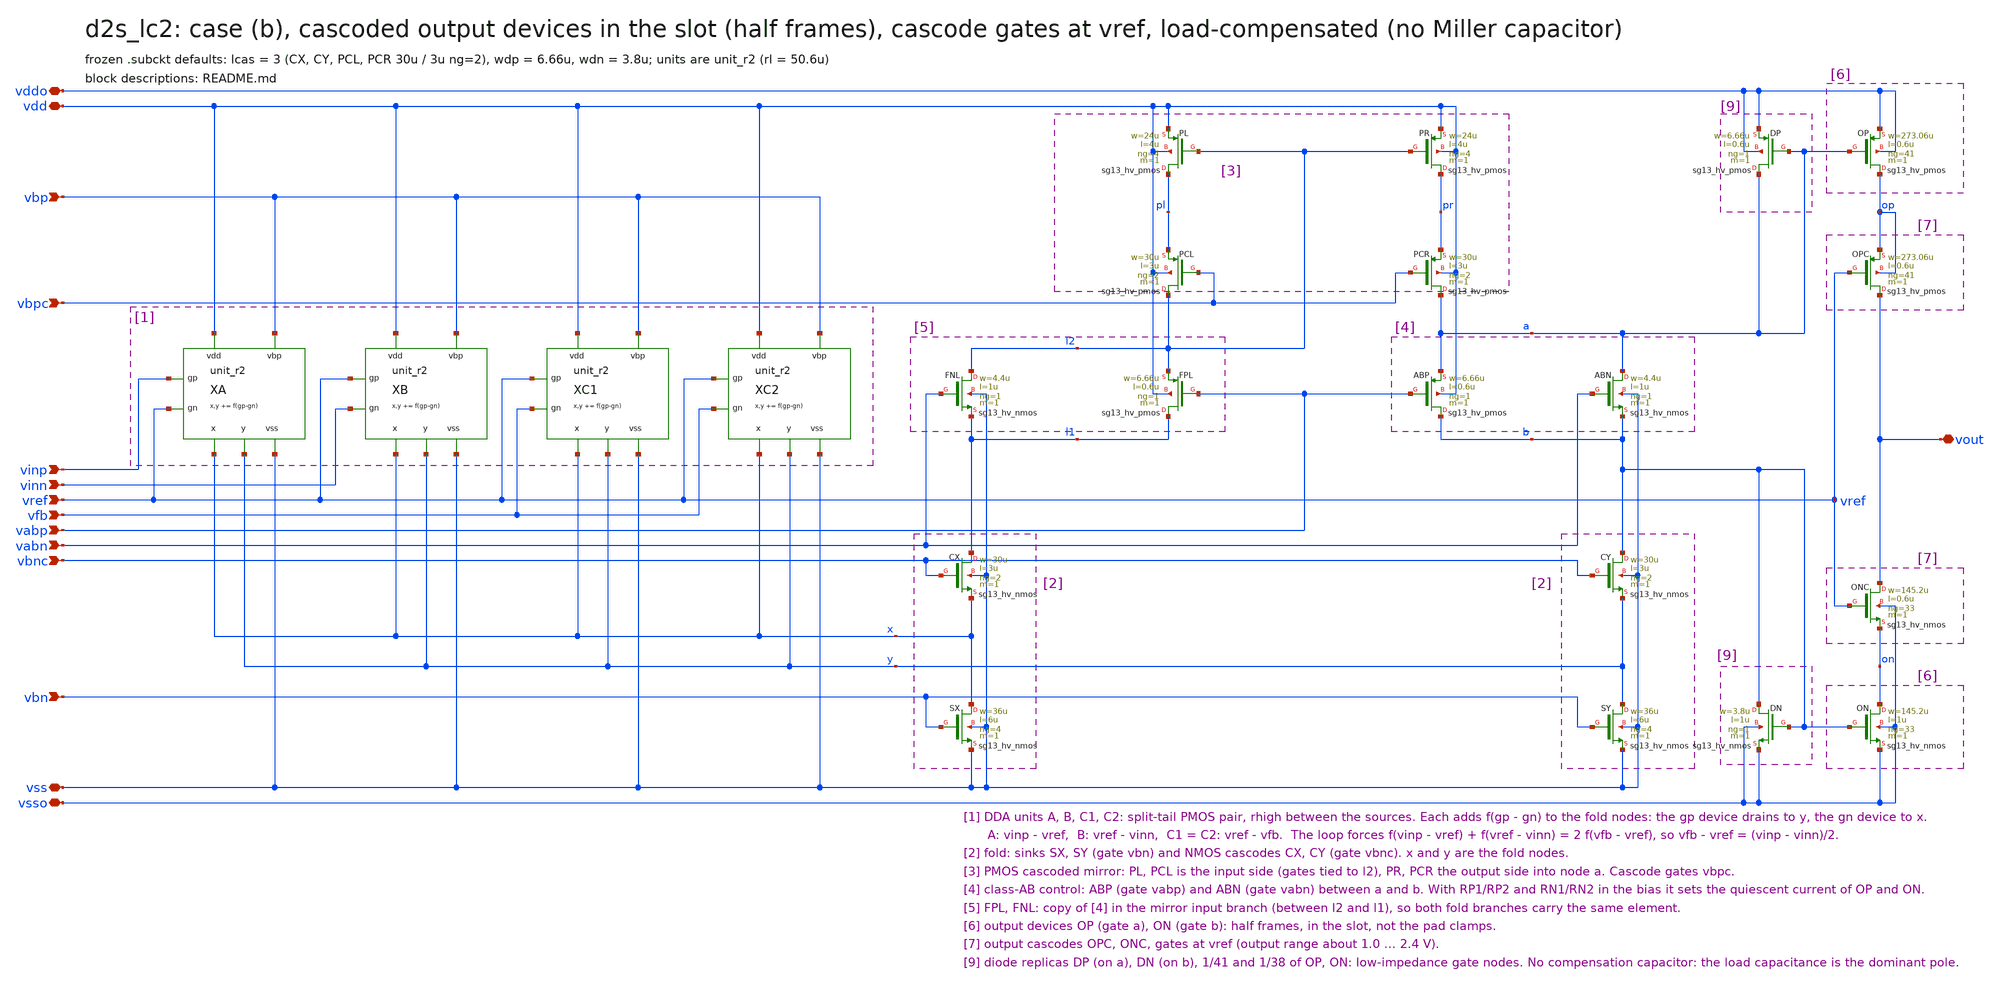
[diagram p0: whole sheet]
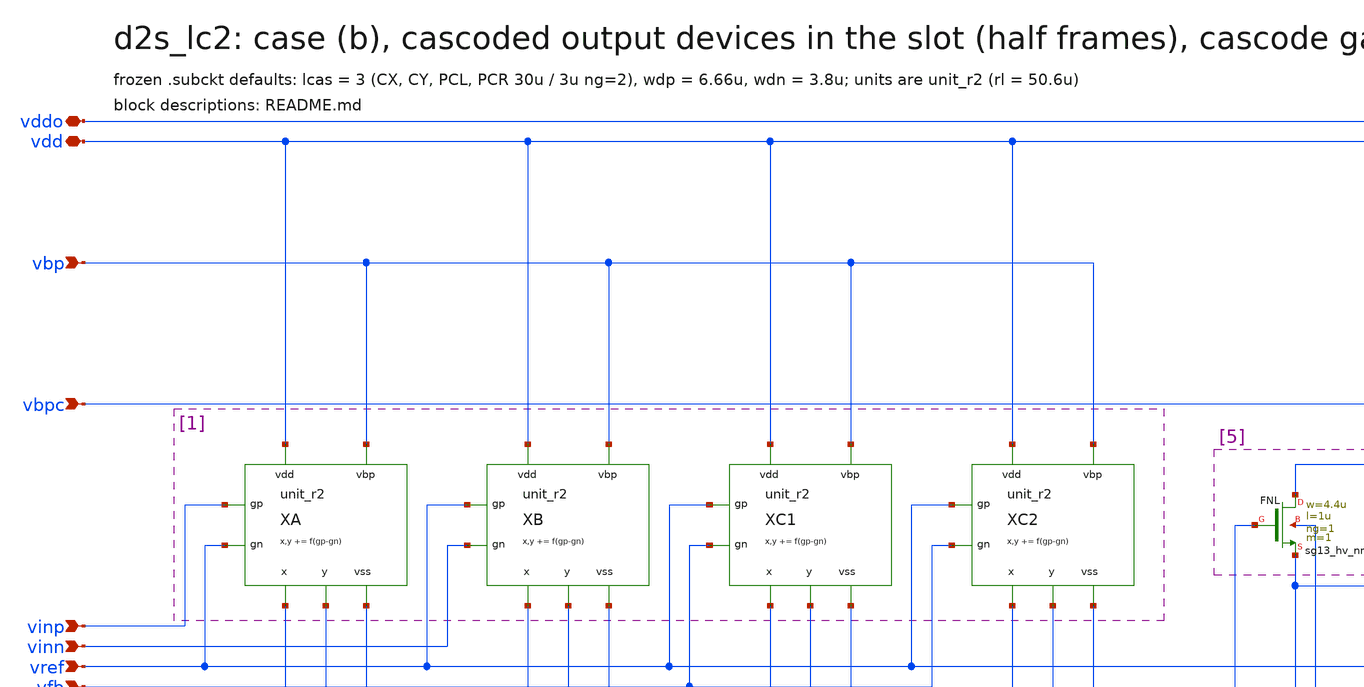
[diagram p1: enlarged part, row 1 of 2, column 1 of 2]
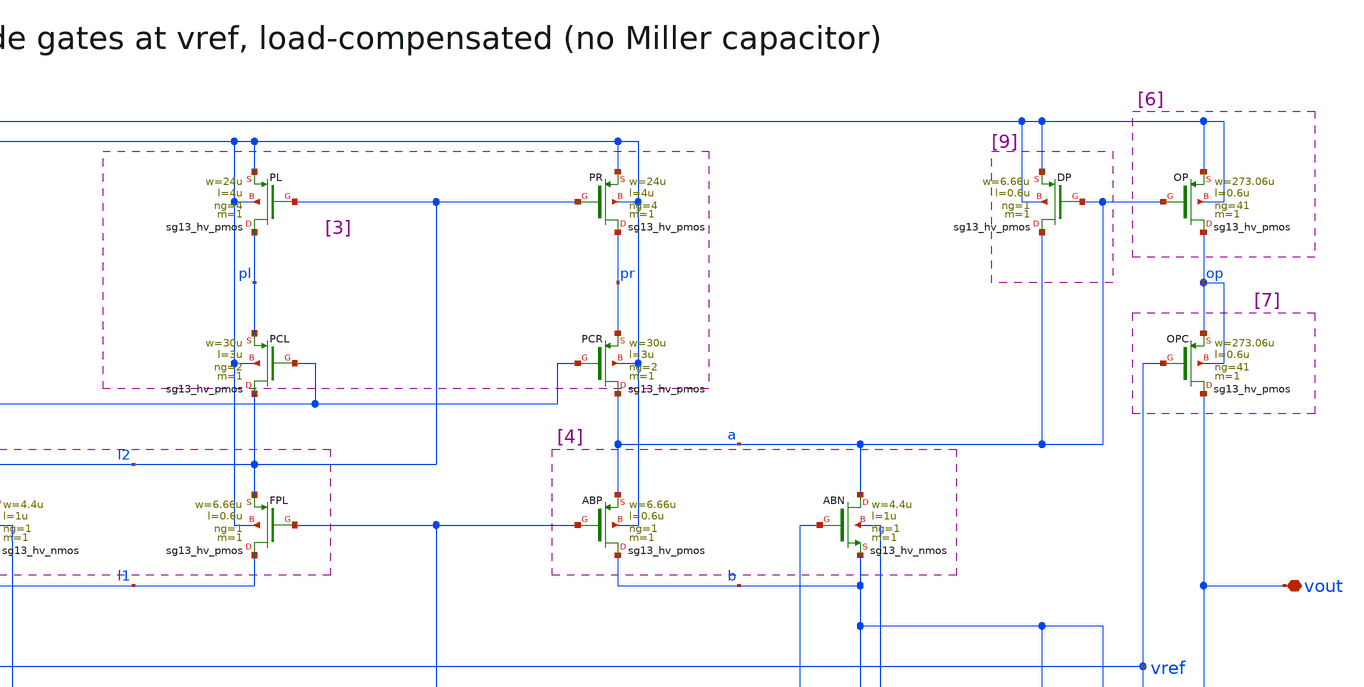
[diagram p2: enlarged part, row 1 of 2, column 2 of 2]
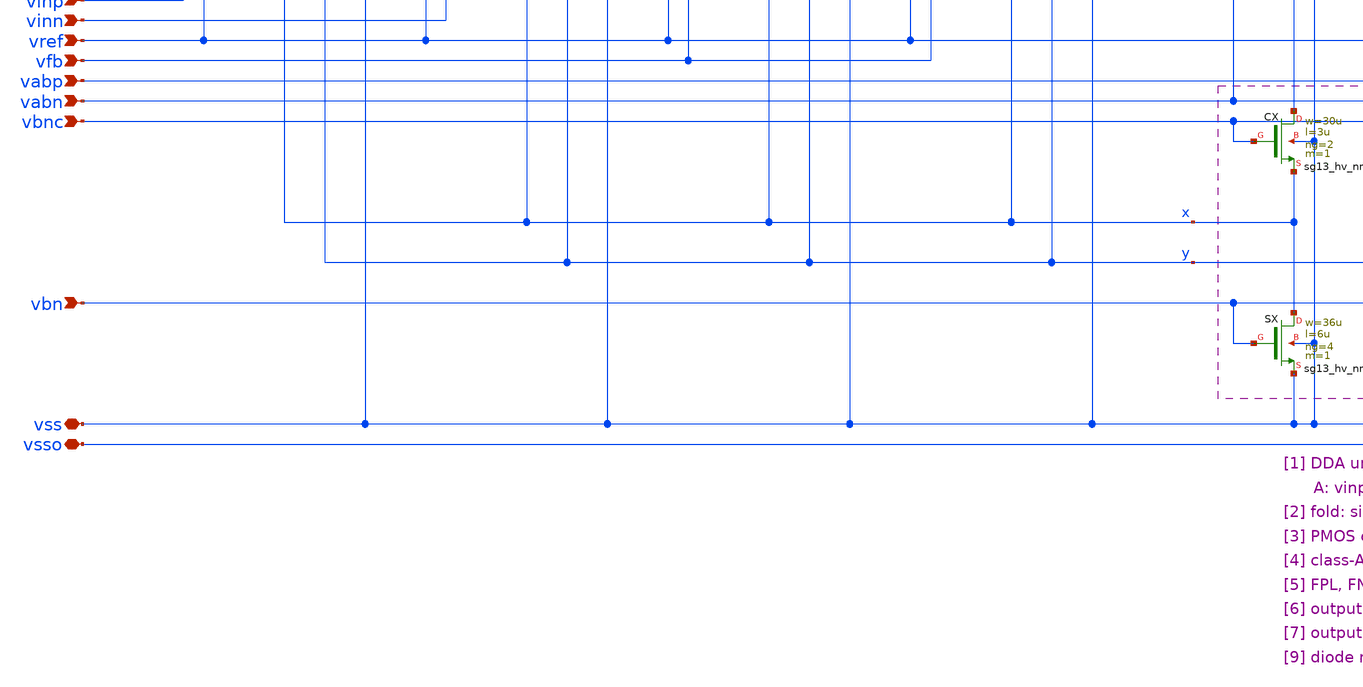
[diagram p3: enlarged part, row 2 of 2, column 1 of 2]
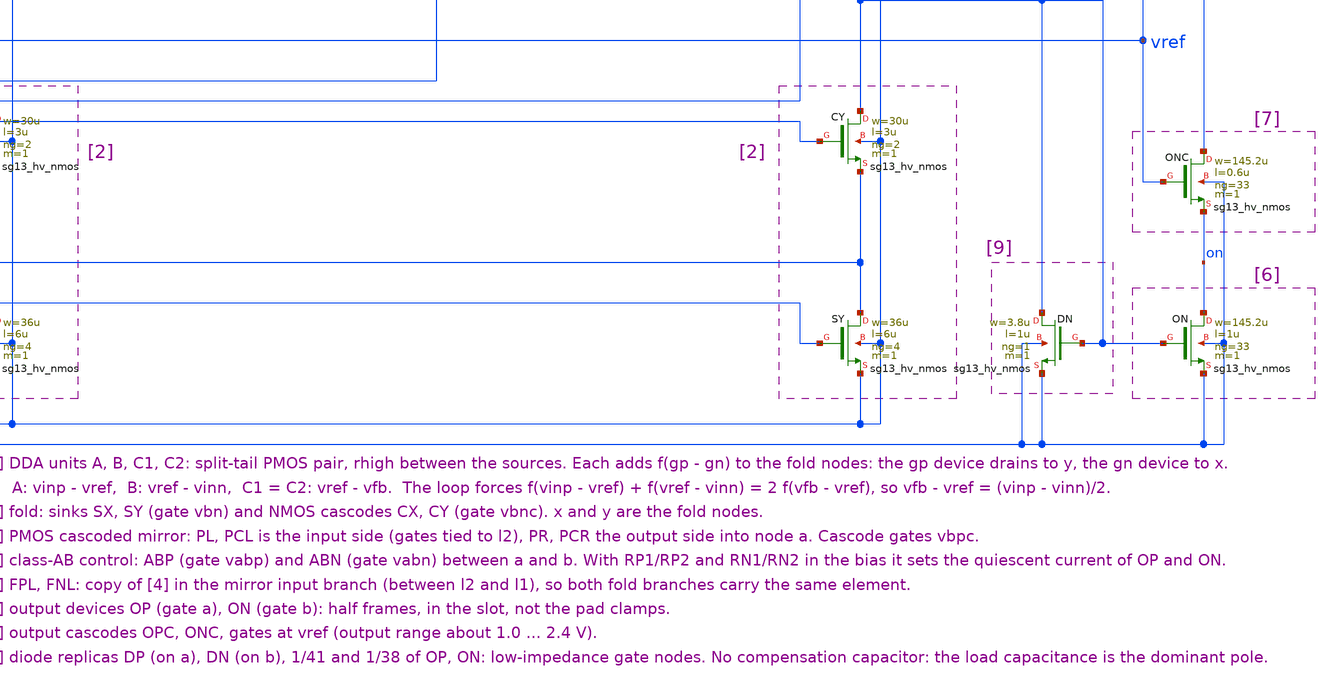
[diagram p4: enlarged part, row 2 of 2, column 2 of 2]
** sch_path: sudelbuecher/design_considerations/class_ab_pad_driver/improvements/xschem/d2s_lc2.sch
**.subckt d2s_lc2 vdd vss vddo vsso vinp vinn vref vout vfb vbp vbn vbpc vbnc vabp vabn
*.iopin vdd
*.iopin vss
*.iopin vddo
*.iopin vsso
*.ipin vinp
*.ipin vinn
*.ipin vref
*.iopin vout
*.ipin vfb
*.ipin vbp
*.ipin vbn
*.ipin vbpc
*.ipin vbnc
*.ipin vabp
*.ipin vabn
XA x y vinp vref vdd vss vbp unit_r2
XB x y vref vinn vdd vss vbp unit_r2
XC1 x y vref vfb vdd vss vbp unit_r2
XC2 x y vref vfb vdd vss vbp unit_r2
XFNL l2 vabn l1 vss sg13_hv_nmos w=4.4u l=1u ng=1 m=1 mm_ok=1
XCX l1 vbnc x vss sg13_hv_nmos w=30u l=3u ng=2 m=1 mm_ok=1
XSX x vbn vss vss sg13_hv_nmos w=36u l=6u ng=4 m=1 mm_ok=1
XPL pl l2 vdd vdd sg13_hv_pmos w=24u l=4u ng=4 m=1 mm_ok=1
XPCL l2 vbpc pl vdd sg13_hv_pmos w=30u l=3u ng=2 m=1 mm_ok=1
XFPL l1 vabp l2 vdd sg13_hv_pmos w=6.66u l=0.6u ng=1 m=1 mm_ok=1
XPR pr l2 vdd vdd sg13_hv_pmos w=24u l=4u ng=4 m=1 mm_ok=1
XPCR a vbpc pr vdd sg13_hv_pmos w=30u l=3u ng=2 m=1 mm_ok=1
XABP b vabp a vdd sg13_hv_pmos w=6.66u l=0.6u ng=1 m=1 mm_ok=1
XABN a vabn b vss sg13_hv_nmos w=4.4u l=1u ng=1 m=1 mm_ok=1
XCY b vbnc y vss sg13_hv_nmos w=30u l=3u ng=2 m=1 mm_ok=1
XSY y vbn vss vss sg13_hv_nmos w=36u l=6u ng=4 m=1 mm_ok=1
XOP op a vddo vddo sg13_hv_pmos w=273.06u l=0.6u ng=41 m=1 mm_ok=1
XOPC vout vref op op sg13_hv_pmos w=273.06u l=0.6u ng=41 m=1 mm_ok=1
XONC vout vref on vsso sg13_hv_nmos w=145.2u l=0.6u ng=33 m=1 mm_ok=1
XON on b vsso vsso sg13_hv_nmos w=145.2u l=1u ng=33 m=1 mm_ok=1
XDP a a vddo vddo sg13_hv_pmos w=6.66u l=0.6u ng=1 m=1 mm_ok=1
XDN b b vsso vsso sg13_hv_nmos w=3.8u l=1u ng=1 m=1 mm_ok=1
**.ends

* expanding   symbol:  unit_r2.sym # of pins=7
** sym_path: sudelbuecher/design_considerations/class_ab_pad_driver/improvements/xschem/unit_r2.sym
** sch_path: sudelbuecher/design_considerations/class_ab_pad_driver/improvements/xschem/unit_r2.sch
.subckt unit_r2 x y gp gn vdd vss vbp
*.opin x
*.opin y
*.ipin gp
*.ipin gn
*.iopin vdd
*.iopin vss
*.ipin vbp
XTa sa vbp vdd vdd sg13_hv_pmos w=5u l=6u ng=1 m=1 mm_ok=1
XTb sb vbp vdd vdd sg13_hv_pmos w=5u l=6u ng=1 m=1 mm_ok=1
XMa y gp sa sa sg13_hv_pmos w=20u l=1u ng=2 m=1 mm_ok=1
XMb x gn sb sb sg13_hv_pmos w=20u l=1u ng=2 m=1 mm_ok=1
XR sa sb vss rhigh w=0.5u l=50.6u m=1 b=0 mm_ok=1
.ends

.end
